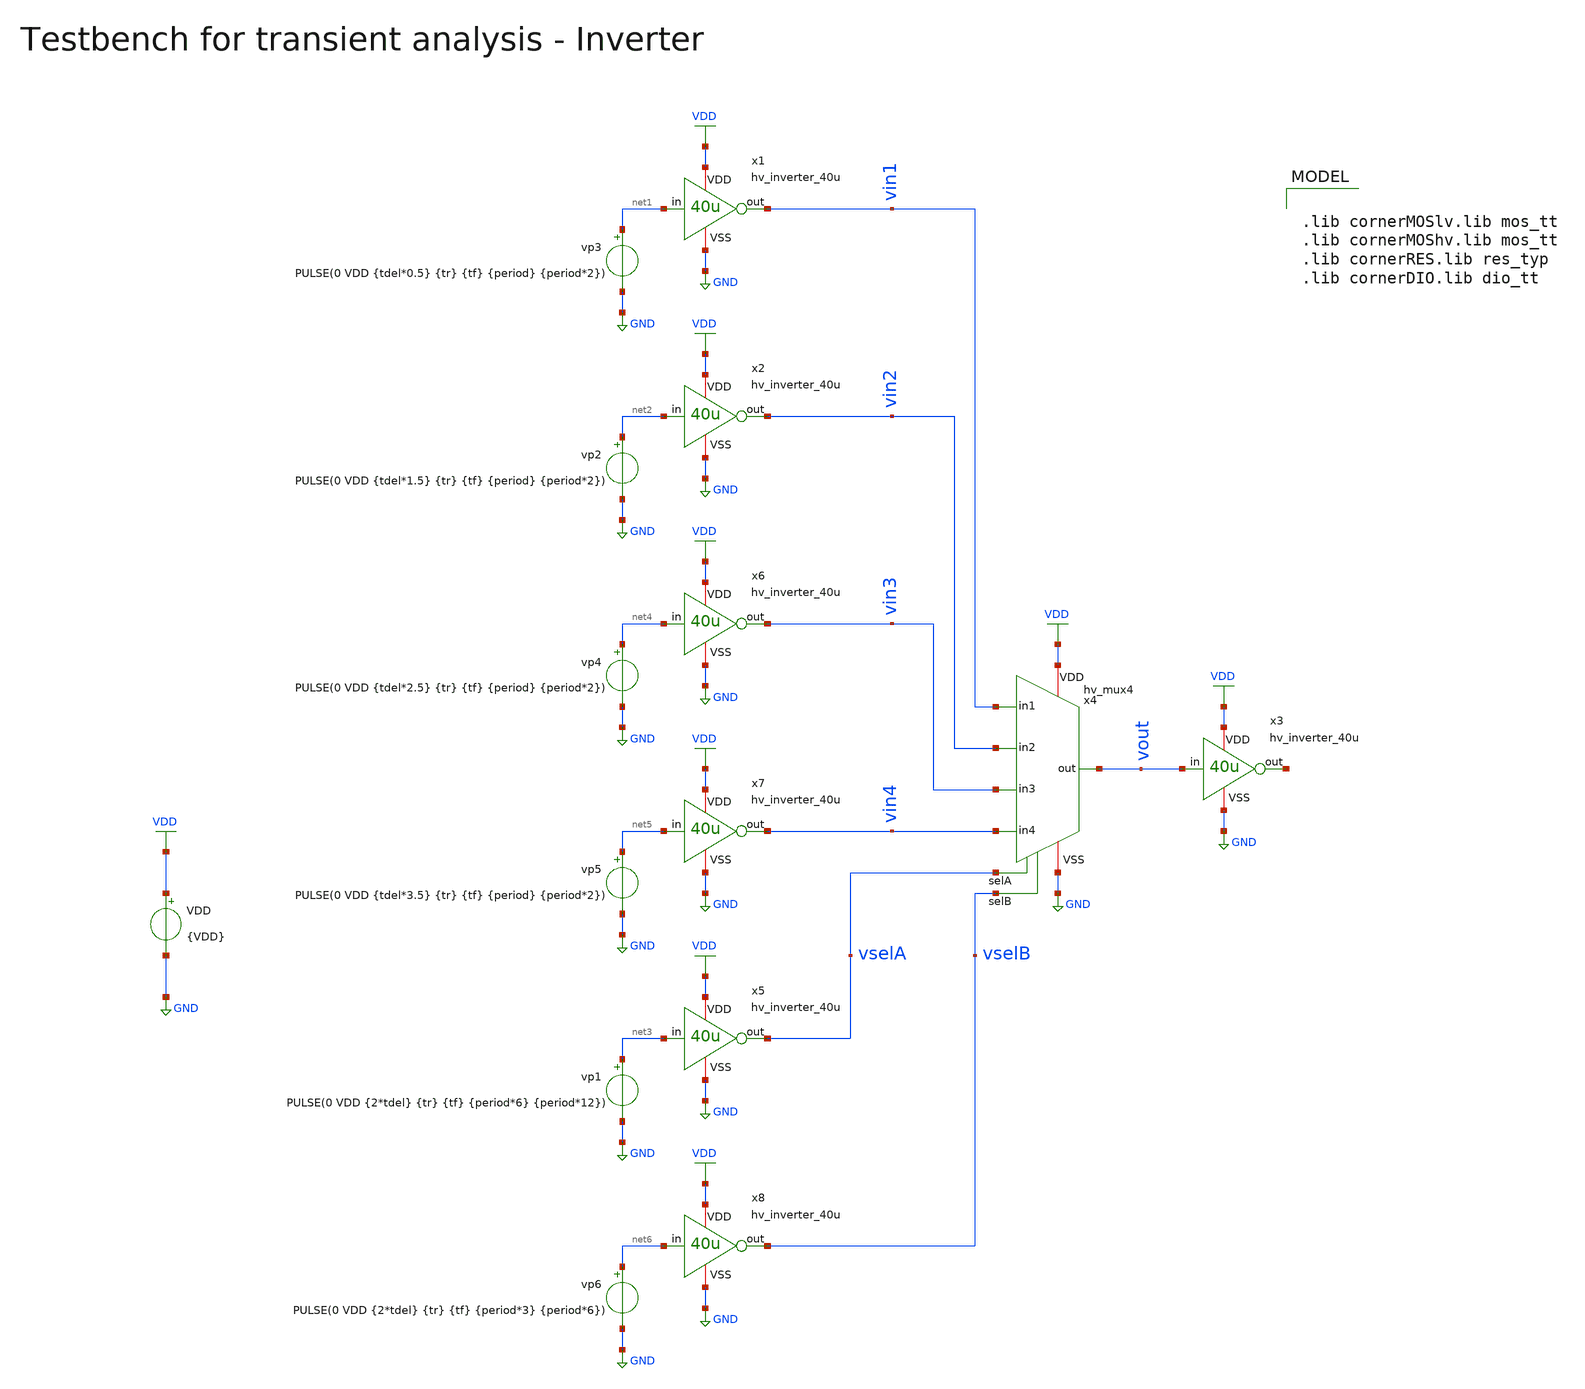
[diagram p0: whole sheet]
** sch_path: macros/heichips26_vcr/macros/switched_capacitor/testbenches/xschem/tb_hv_mux4_tran.sch
**.subckt tb_hv_mux4_tran
VDD VDD GND {VDD}
vp2 net2 GND PULSE(0 VDD {tdel*1.5} {tr} {tf} {period} {period*2})
vp1 net3 GND PULSE(0 VDD {2*tdel} {tr} {tf} {period*6} {period*12})
x1 VDD net1 vin1 GND hv_inverter_40u
x2 VDD net2 vin2 GND hv_inverter_40u
x3 VDD vout net7 GND hv_inverter_40u
vp3 net1 GND PULSE(0 VDD {tdel*0.5} {tr} {tf} {period} {period*2})
x5 VDD net3 vselA GND hv_inverter_40u
vp4 net4 GND PULSE(0 VDD {tdel*2.5} {tr} {tf} {period} {period*2})
x6 VDD net4 vin3 GND hv_inverter_40u
vp5 net5 GND PULSE(0 VDD {tdel*3.5} {tr} {tf} {period} {period*2})
x7 VDD net5 vin4 GND hv_inverter_40u
vp6 net6 GND PULSE(0 VDD {2*tdel} {tr} {tf} {period*3} {period*6})
x8 VDD net6 vselB GND hv_inverter_40u
x4 vselA VDD vout GND vin3 vin1 vin4 vin2 vselB hv_mux4
**** begin user architecture code


.param VDD=3.3
.csparam VDD=VDD
.param Vcm=VDD/2
.param temp=27
.param Cload=10p
.param Rload=1k

.param period = 10n
.param tdel   = {period/4}
.param ton    = {period*2}
.csparam tstop  = {13*period}
.csparam tstep  = {period/100}
.param tr     = {period/100}
.param tf     = {period/100}

.options savecurrents klu method=gear reltol=1e-4 abstol=1e-15 gmin=1e-15
.control

save all

* Operating Point Analysis
op
remzerovec
write @schname\.raw
set appendwrite

* Transient Analysis
tran {$&tstep} {$&tstop}
write @schname\.raw

* Plotting
plot vselA+24 vselB+20 vin1+16 vin2+12 vin3+8 vin4+4 vout

* Write Data
unset appendwrite
set wr_vecnames
set wr_singlescale
wrdata ../plot_simulations/data/@schname\.txt v(vin1) v(vin2) v(vout)

*quit
.endc



.lib cornerMOSlv.lib mos_tt
.lib cornerMOShv.lib mos_tt
.lib cornerRES.lib res_typ
.lib cornerDIO.lib dio_tt

**** end user architecture code
**.ends
.GLOBAL GND
.GLOBAL VDD
.end
